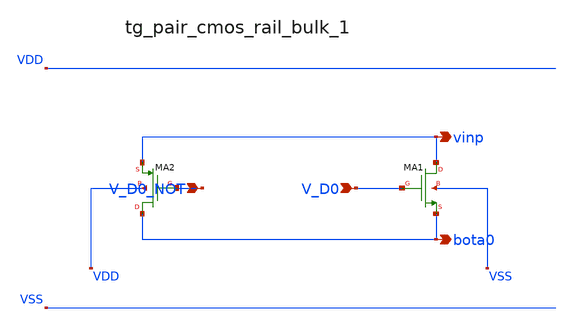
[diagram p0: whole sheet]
** sch_path: analog-db/raw/ia_005_hsu_pga_ideal/hier/blocks/tg_pair_cmos_rail_bulk_1.sch
**.subckt tg_pair_cmos_rail_bulk_1 V_D0_NOT V_D0 vinp bota0
*.ipin V_D0_NOT
*.ipin V_D0
*.opin vinp
*.opin bota0
XMA1 vinp V_D0 bota0 VSS sg13_lv_nmos w=x_dut_xma1_w l=x_dut_xma1_l ng=1 m=x_dut_xma1_m
XMA2 bota0 V_D0_NOT vinp VDD sg13_lv_pmos w=x_dut_xma2_w l=x_dut_xma2_l ng=1 m=x_dut_xma2_m
**.ends
.end
